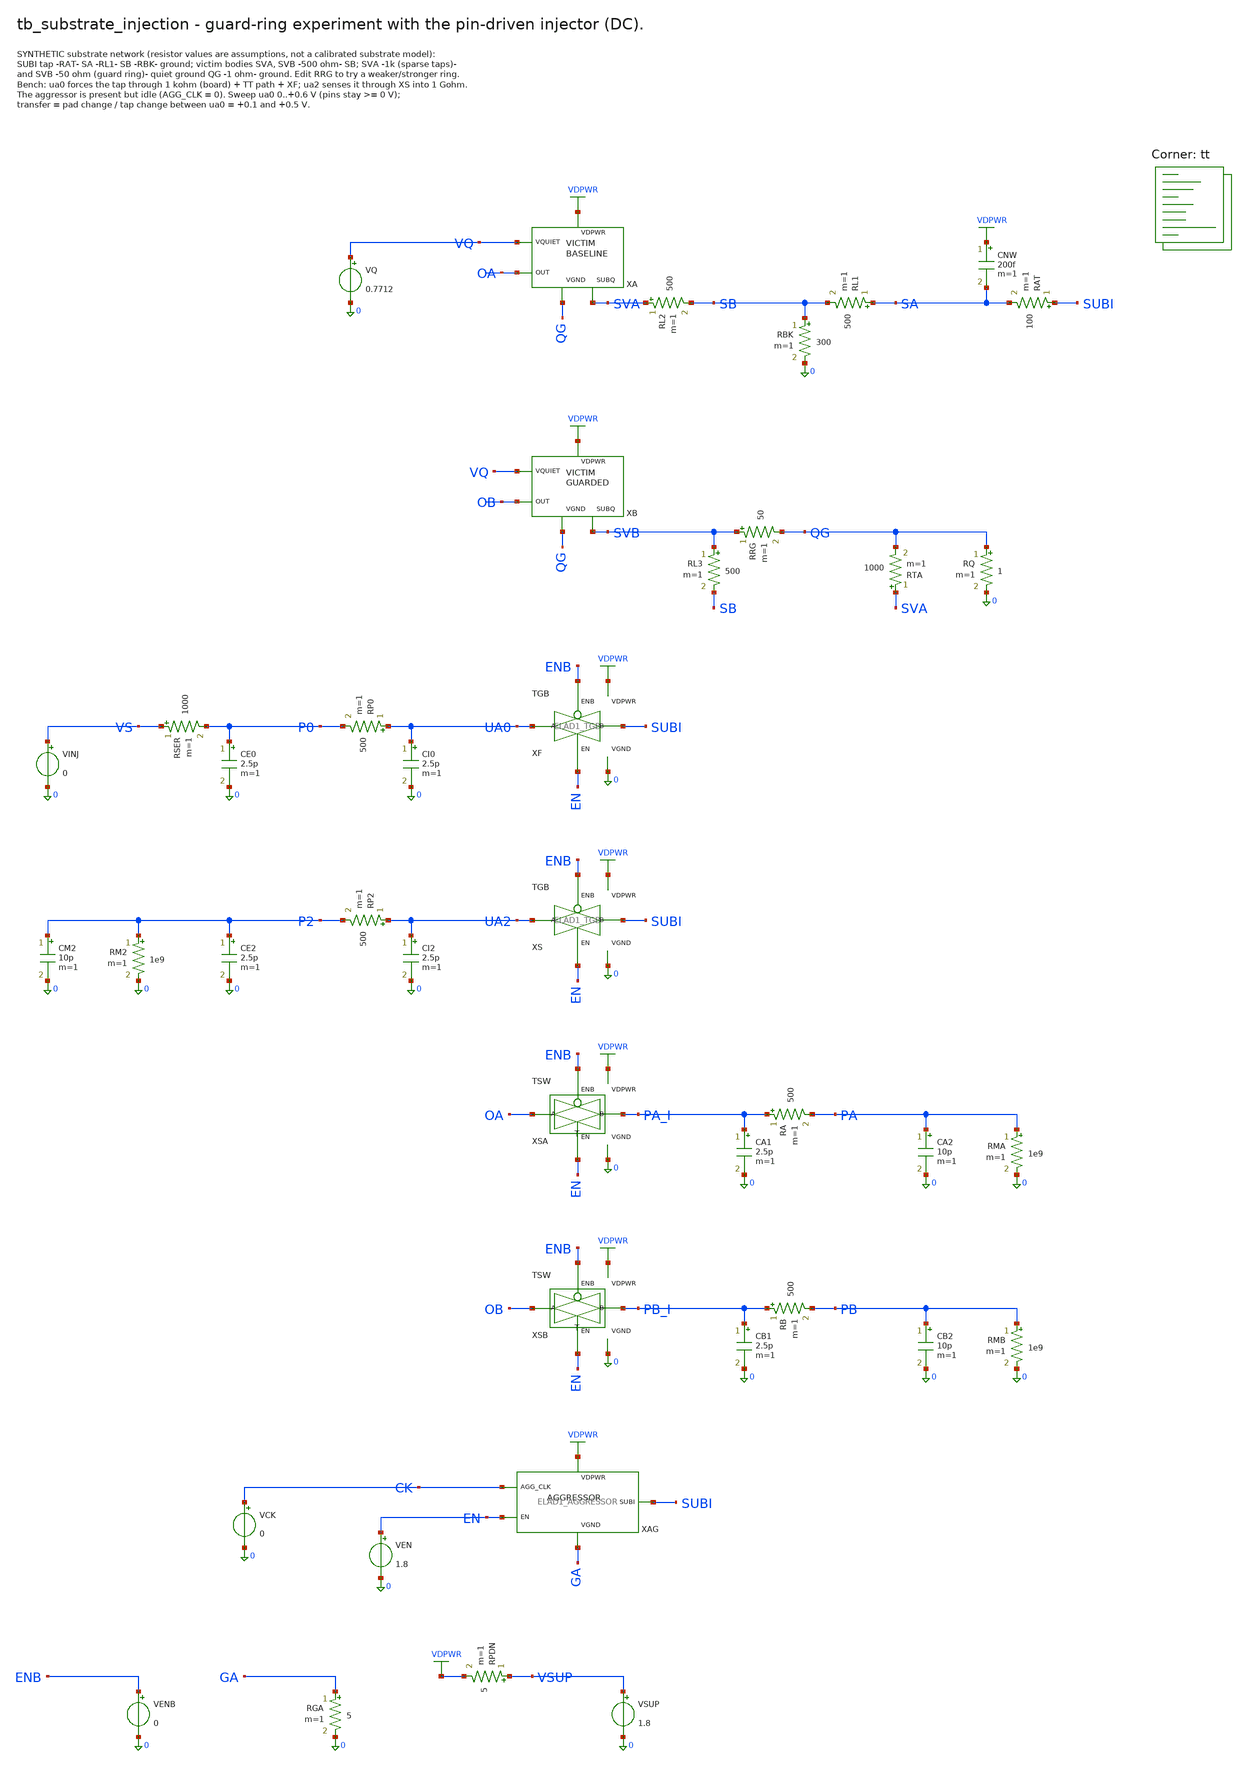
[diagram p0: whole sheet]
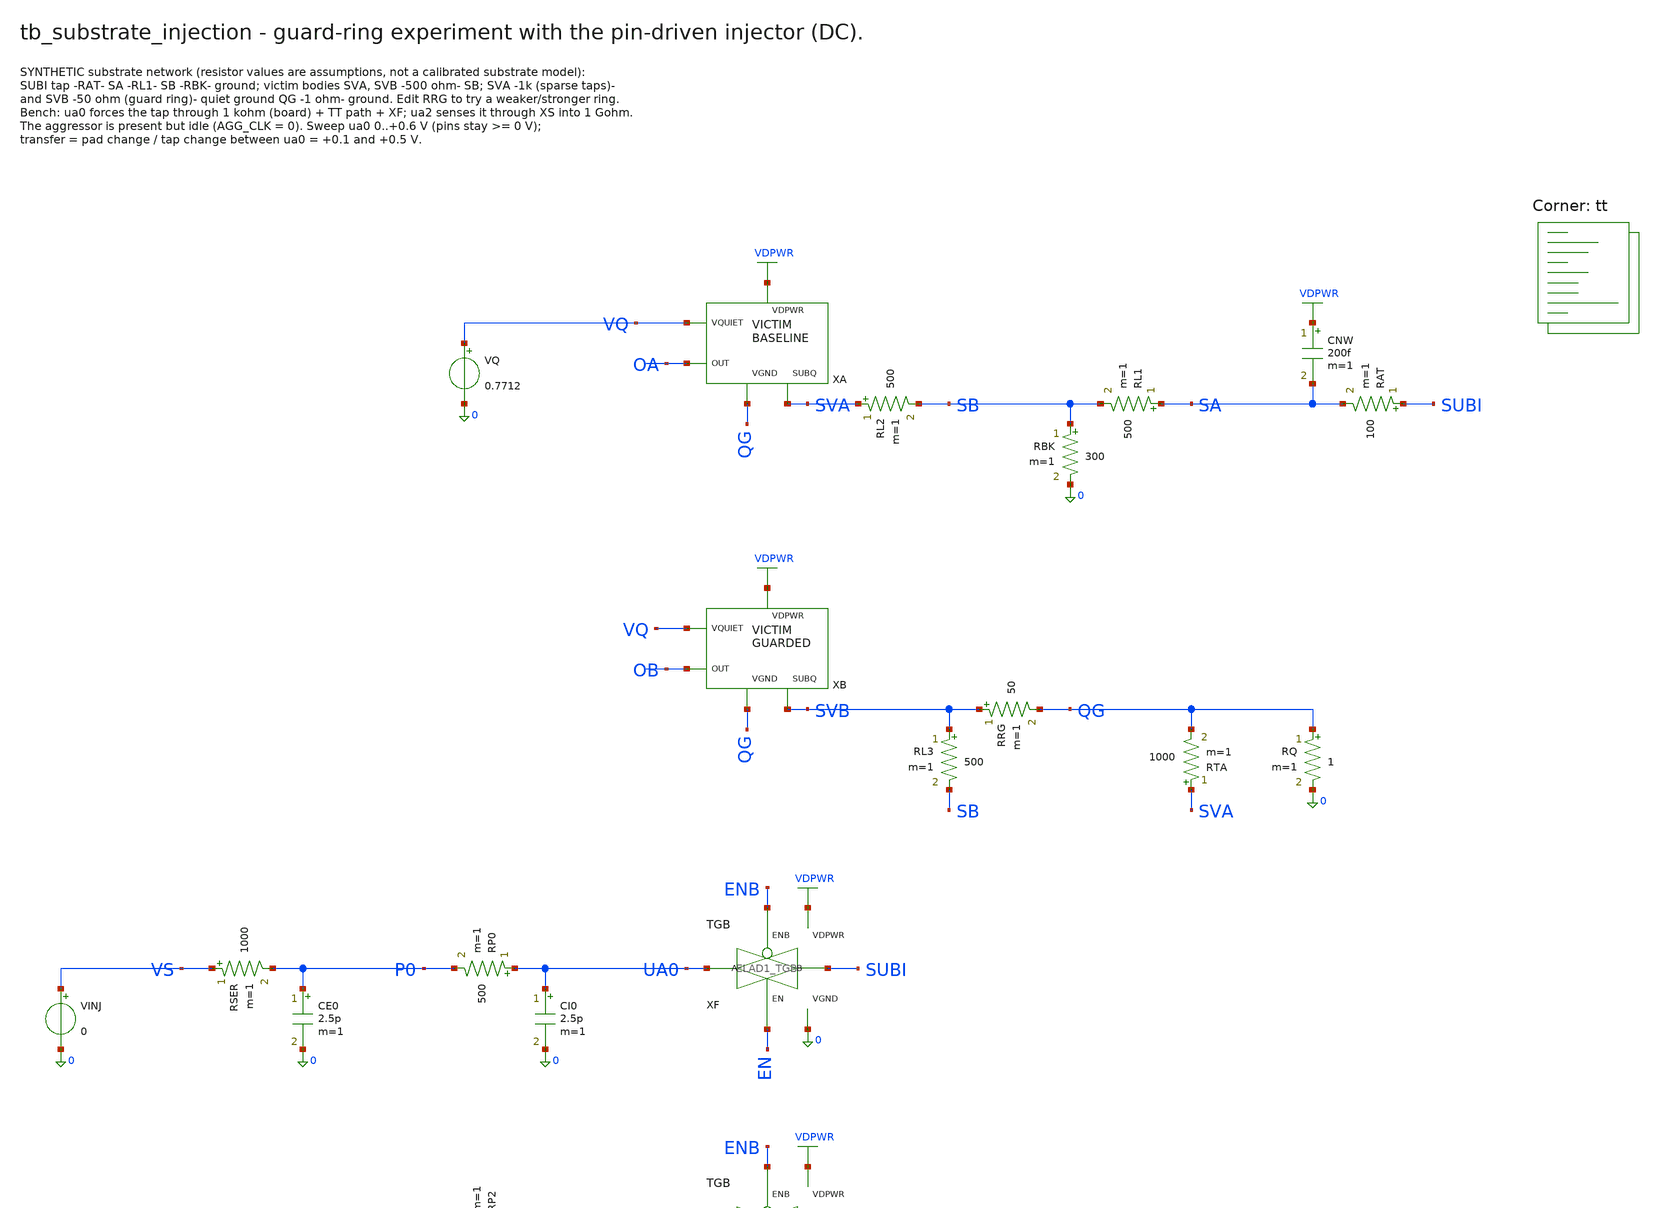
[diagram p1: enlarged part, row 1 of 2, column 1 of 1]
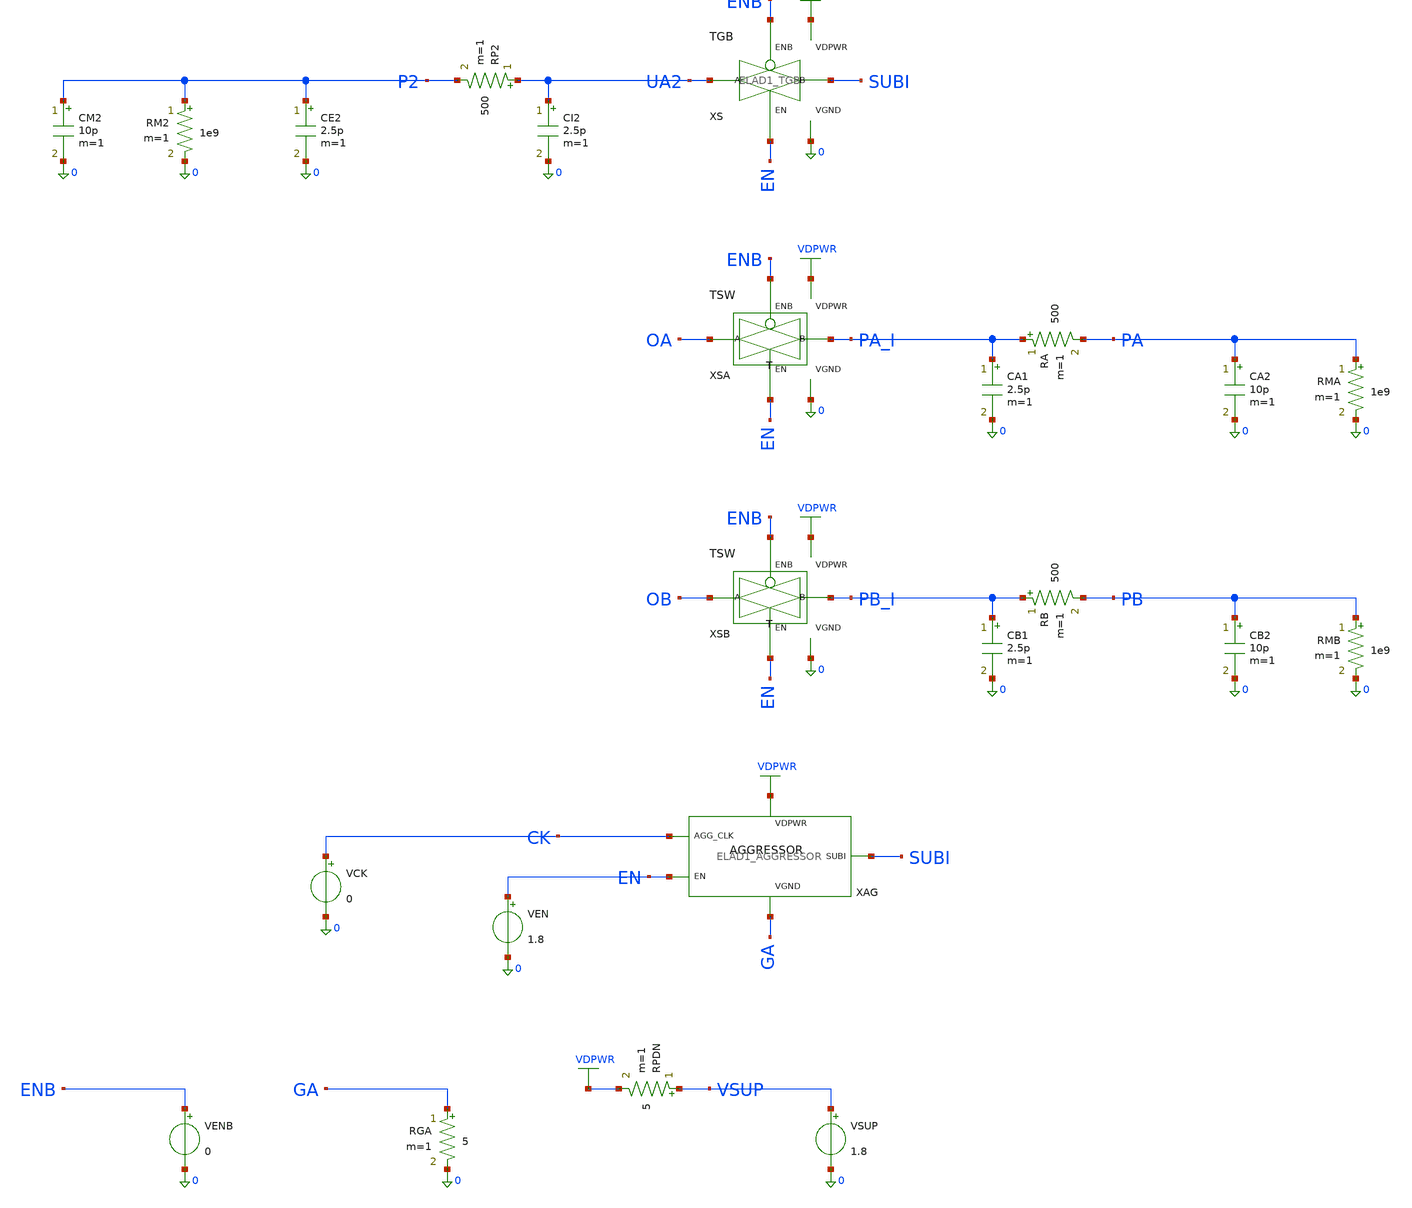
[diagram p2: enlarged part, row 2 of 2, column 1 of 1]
** sch_path: cells/ELAD1_AGGRESSOR/schematic/tb_substrate_injection.sch
**.subckt tb_substrate_injection
XA VQ OA VDPWR QG SVA ELAD1_VICTIM_BASELINE
VQ VQ 0 0.7712
RL2 SVA SB 500 m=1
RBK SB 0 300 m=1
RL1 SA SB 500 m=1
CNW VDPWR SA 200f m=1
RAT SUBI SA 100 m=1
XB VQ OB VDPWR QG SVB ELAD1_VICTIM_GUARDED
RL3 SVB SB 500 m=1
RRG SVB QG 50 m=1
RTA SVA QG 1000 m=1
RQ QG 0 1 m=1
XF UA0 SUBI EN ENB VDPWR 0 ELAD1_TGB
CI0 UA0 0 2.5p m=1
RP0 UA0 P0 500 m=1
CE0 P0 0 2.5p m=1
RSER VS P0 1000 m=1
VINJ VS 0 0
XS UA2 SUBI EN ENB VDPWR 0 ELAD1_TGB
CI2 UA2 0 2.5p m=1
RP2 UA2 P2 500 m=1
CE2 P2 0 2.5p m=1
RM2 P2 0 1e9 m=1
CM2 P2 0 10p m=1
XSA OA PA_I EN ENB VDPWR 0 ELAD1_TSW
CA1 PA_I 0 2.5p m=1
RA PA_I PA 500 m=1
CA2 PA 0 10p m=1
RMA PA 0 1e9 m=1
XSB OB PB_I EN ENB VDPWR 0 ELAD1_TSW
CB1 PB_I 0 2.5p m=1
RB PB_I PB 500 m=1
CB2 PB 0 10p m=1
RMB PB 0 1e9 m=1
XAG CK EN VDPWR GA SUBI ELAD1_AGGRESSOR
VEN EN 0 1.8
VCK CK 0 0
VENB ENB 0 0
RGA GA 0 5 m=1
RPDN VSUP VDPWR 5 m=1
VSUP VSUP 0 1.8
**** begin user architecture code

.option gmin=1e-15 reltol=1e-6 abstol=1e-15 vntol=1e-8
.control
dc VINJ 0 0.6 0.05
meas dc ph find v(P2) at=0.5
meas dc pl find v(P2) at=0.1
meas dc th find v(SUBI) at=0.5
meas dc ah find v(PA) at=0.5
meas dc al find v(PA) at=0.1
meas dc bh find v(PB) at=0.5
meas dc bl find v(PB) at=0.1
meas dc z find v(SUBI) at=0
let t_a = (ah-al)/(ph-pl)
let t_b = (bh-bl)/(ph-pl)
let ratio = t_a/t_b
let sense_err = abs(ph-th)
let tap0 = abs(z)
echo ROW inject tap_hi=$&ph t_a=$&t_a t_b=$&t_b ratio=$&ratio sense_err=$&sense_err tap0=$&tap0
.endc

.lib $::SKYWATER_MODELS/sky130.lib.spice tt
**** end user architecture code
**.ends

* expanding   symbol:  ELAD1_VICTIM_BASELINE.sym # of pins=5
** sym_path: cells/ELAD1_VICTIM_BASELINE/schematic/ELAD1_VICTIM_BASELINE.sym
** sch_path: cells/ELAD1_VICTIM_BASELINE/schematic/ELAD1_VICTIM_BASELINE.sch
.subckt ELAD1_VICTIM_BASELINE VQUIET OUT VDPWR VGND SUBQ
*.iopin VQUIET
*.iopin OUT
*.iopin VDPWR
*.iopin VGND
*.iopin SUBQ
XMVIC[1] OUT VQUIET VGND SUBQ sky130_fd_pr__nfet_01v8 L=1 W=1 nf=1 ad='int((1 + 1)/2) * 1 / 1 * 0.29'
+ as='int((1 + 2)/2) * 1 / 1 * 0.29' pd='2*int((1 + 1)/2) * (1 / 1 + 0.29)' ps='2*int((1 + 2)/2) * (1 / 1 + 0.29)'
+ nrd='0.29 / 1 ' nrs='0.29 / 1 ' sa=0 sb=0 sd=0 mult=1 m=1
XMVIC[0] OUT VQUIET VGND SUBQ sky130_fd_pr__nfet_01v8 L=1 W=1 nf=1 ad='int((1 + 1)/2) * 1 / 1 * 0.29'
+ as='int((1 + 2)/2) * 1 / 1 * 0.29' pd='2*int((1 + 1)/2) * (1 / 1 + 0.29)' ps='2*int((1 + 2)/2) * (1 / 1 + 0.29)'
+ nrd='0.29 / 1 ' nrs='0.29 / 1 ' sa=0 sb=0 sd=0 mult=1 m=1
XMD[1] VGND VGND VGND SUBQ sky130_fd_pr__nfet_01v8 L=1 W=1 nf=1 ad='int((1 + 1)/2) * 1 / 1 * 0.29' as='int((1 + 2)/2) * 1 / 1 * 0.29'
+ pd='2*int((1 + 1)/2) * (1 / 1 + 0.29)' ps='2*int((1 + 2)/2) * (1 / 1 + 0.29)' nrd='0.29 / 1 ' nrs='0.29 / 1 '
+ sa=0 sb=0 sd=0 mult=2 m=2
XMD[0] VGND VGND VGND SUBQ sky130_fd_pr__nfet_01v8 L=1 W=1 nf=1 ad='int((1 + 1)/2) * 1 / 1 * 0.29' as='int((1 + 2)/2) * 1 / 1 * 0.29'
+ pd='2*int((1 + 1)/2) * (1 / 1 + 0.29)' ps='2*int((1 + 2)/2) * (1 / 1 + 0.29)' nrd='0.29 / 1 ' nrs='0.29 / 1 '
+ sa=0 sb=0 sd=0 mult=2 m=2
XR1 OUT VDPWR SUBQ sky130_fd_pr__res_xhigh_po_0p69 L=31.7 mult=1 m=1
.ends


* expanding   symbol:  ELAD1_VICTIM_GUARDED.sym # of pins=5
** sym_path: cells/ELAD1_VICTIM_GUARDED/schematic/ELAD1_VICTIM_GUARDED.sym
** sch_path: cells/ELAD1_VICTIM_GUARDED/schematic/ELAD1_VICTIM_GUARDED.sch
.subckt ELAD1_VICTIM_GUARDED VQUIET OUT VDPWR VGND SUBQ
*.iopin VQUIET
*.iopin OUT
*.iopin VDPWR
*.iopin VGND
*.iopin SUBQ
XRLD VDPWR OUT SUBQ sky130_fd_pr__res_xhigh_po W=0.69 L=31.7 mult=1 m=1
XMVIC OUT VQUIET VGND SUBQ sky130_fd_pr__nfet_01v8 L=1 W=2 nf=1 ad='int((1 + 1)/2) * 2 / 1 * 0.29' as='int((1 + 2)/2) * 2 / 1 * 0.29'
+ pd='2*int((1 + 1)/2) * (2 / 1 + 0.29)' ps='2*int((1 + 2)/2) * (2 / 1 + 0.29)' nrd='0.29 / 2 ' nrs='0.29 / 2 '
+ sa=0 sb=0 sd=0 mult=1 m=1
XDUM[1] VGND VGND VGND SUBQ sky130_fd_pr__nfet_01v8 L=1 W=2 nf=1 ad='int((1 + 1)/2) * 2 / 1 * 0.29' as='int((1 + 2)/2) * 2 / 1 * 0.29'
+ pd='2*int((1 + 1)/2) * (2 / 1 + 0.29)' ps='2*int((1 + 2)/2) * (2 / 1 + 0.29)' nrd='0.29 / 2 ' nrs='0.29 / 2 '
+ sa=0 sb=0 sd=0 mult=1 m=1
XDUM[0] VGND VGND VGND SUBQ sky130_fd_pr__nfet_01v8 L=1 W=2 nf=1 ad='int((1 + 1)/2) * 2 / 1 * 0.29' as='int((1 + 2)/2) * 2 / 1 * 0.29'
+ pd='2*int((1 + 1)/2) * (2 / 1 + 0.29)' ps='2*int((1 + 2)/2) * (2 / 1 + 0.29)' nrd='0.29 / 2 ' nrs='0.29 / 2 '
+ sa=0 sb=0 sd=0 mult=1 m=1
.ends


* expanding   symbol:  ELAD1_TGB.sym # of pins=6
** sym_path: cells/ELAD1_TGB/schematic/ELAD1_TGB.sym
** sch_path: cells/ELAD1_TGB/schematic/ELAD1_TGB.sch
.subckt ELAD1_TGB A B EN ENB VDPWR VGND
*.iopin A
*.iopin B
*.iopin EN
*.iopin ENB
*.iopin VDPWR
*.iopin VGND
XMN A EN B VGND sky130_fd_pr__nfet_01v8 L=0.15 W=1 nf=1 ad='int((1 + 1)/2) * 1 / 1 * 0.29' as='int((1 + 2)/2) * 1 / 1 * 0.29'
+ pd='2*int((1 + 1)/2) * (1 / 1 + 0.29)' ps='2*int((1 + 2)/2) * (1 / 1 + 0.29)' nrd='0.29 / 1 ' nrs='0.29 / 1 '
+ sa=0 sb=0 sd=0 mult=1 m=1
XMP A ENB B VDPWR sky130_fd_pr__pfet_01v8 L=0.15 W=2 nf=1 ad='int((nf+1)/2) * W/nf * 0.29' as='int((nf+2)/2) * W/nf * 0.29'
+ pd='2*int((nf+1)/2) * (W/nf + 0.29)' ps='2*int((nf+2)/2) * (W/nf + 0.29)' nrd='0.29 / W' nrs='0.29 / W'
+ sa=0 sb=0 sd=0 mult=1 m=1
.ends


* expanding   symbol:  ELAD1_TSW.sym # of pins=6
** sym_path: cells/ELAD1_TSW/schematic/ELAD1_TSW.sym
** sch_path: cells/ELAD1_TSW/schematic/ELAD1_TSW.sch
.subckt ELAD1_TSW A B EN ENB VDPWR VGND
*.iopin A
*.iopin B
*.iopin EN
*.iopin ENB
*.iopin VDPWR
*.iopin VGND
x1 A M EN ENB VDPWR VGND ELAD1_TGA
x1 M B EN ENB VDPWR VGND ELAD1_TGA
XMN1 M ENB VGND VGND sky130_fd_pr__nfet_01v8 L=0.15 W=1 nf=1 ad='int((1 + 1)/2) * 1 / 1 * 0.29' as='int((1 + 2)/2) * 1 / 1 * 0.29'
+ pd='2*int((1 + 1)/2) * (1 / 1 + 0.29)' ps='2*int((1 + 2)/2) * (1 / 1 + 0.29)' nrd='0.29 / 1 ' nrs='0.29 / 1 '
+ sa=0 sb=0 sd=0 mult=1 m=1
.ends


* expanding   symbol:  ELAD1_AGGRESSOR.sym # of pins=5
** sym_path: cells/ELAD1_AGGRESSOR/schematic/ELAD1_AGGRESSOR.sym
** sch_path: cells/ELAD1_AGGRESSOR/schematic/ELAD1_AGGRESSOR.sch
.subckt ELAD1_AGGRESSOR AGG_CLK EN VDPWR VGND SUBI
*.iopin AGG_CLK
*.iopin EN
*.iopin VDPWR
*.iopin VGND
*.iopin SUBI
XIC AGG_CLK CKB VDPWR VGND ELAD1_INV
XIE EN ENB VDPWR VGND ELAD1_INV
XGIP1 gip ENB VDPWR VDPWR sky130_fd_pr__pfet_01v8 L=0.15 W=2 nf=1 ad='int((nf+1)/2) * W/nf * 0.29' as='int((nf+2)/2) * W/nf * 0.29'
+ pd='2*int((nf+1)/2) * (W/nf + 0.29)' ps='2*int((nf+2)/2) * (W/nf + 0.29)' nrd='0.29 / W' nrs='0.29 / W'
+ sa=0 sb=0 sd=0 mult=1 m=1
XGIP2 GI CKB gip VDPWR sky130_fd_pr__pfet_01v8 L=0.15 W=2 nf=1 ad='int((nf+1)/2) * W/nf * 0.29' as='int((nf+2)/2) * W/nf * 0.29'
+ pd='2*int((nf+1)/2) * (W/nf + 0.29)' ps='2*int((nf+2)/2) * (W/nf + 0.29)' nrd='0.29 / W' nrs='0.29 / W'
+ sa=0 sb=0 sd=0 mult=1 m=1
XGIN1 GI ENB VGND VGND sky130_fd_pr__nfet_01v8 L=1 W=0.42 nf=1 ad='int((1 + 1)/2) * 0.42 / 1 * 0.29'
+ as='int((1 + 2)/2) * 0.42 / 1 * 0.29' pd='2*int((1 + 1)/2) * (0.42 / 1 + 0.29)' ps='2*int((1 + 2)/2) * (0.42 / 1 + 0.29)'
+ nrd='0.29 / 0.42 ' nrs='0.29 / 0.42 ' sa=0 sb=0 sd=0 mult=1 m=1
XGIN2 GI CKB VGND VGND sky130_fd_pr__nfet_01v8 L=1 W=0.42 nf=1 ad='int((1 + 1)/2) * 0.42 / 1 * 0.29'
+ as='int((1 + 2)/2) * 0.42 / 1 * 0.29' pd='2*int((1 + 1)/2) * (0.42 / 1 + 0.29)' ps='2*int((1 + 2)/2) * (0.42 / 1 + 0.29)'
+ nrd='0.29 / 0.42 ' nrs='0.29 / 0.42 ' sa=0 sb=0 sd=0 mult=1 m=1
XGDP1 gdp ENB VDPWR VDPWR sky130_fd_pr__pfet_01v8 L=0.15 W=2 nf=1 ad='int((nf+1)/2) * W/nf * 0.29' as='int((nf+2)/2) * W/nf * 0.29'
+ pd='2*int((nf+1)/2) * (W/nf + 0.29)' ps='2*int((nf+2)/2) * (W/nf + 0.29)' nrd='0.29 / W' nrs='0.29 / W'
+ sa=0 sb=0 sd=0 mult=1 m=1
XGDP2 GD AGG_CLK gdp VDPWR sky130_fd_pr__pfet_01v8 L=0.15 W=2 nf=1 ad='int((nf+1)/2) * W/nf * 0.29' as='int((nf+2)/2) * W/nf * 0.29'
+ pd='2*int((nf+1)/2) * (W/nf + 0.29)' ps='2*int((nf+2)/2) * (W/nf + 0.29)' nrd='0.29 / W' nrs='0.29 / W'
+ sa=0 sb=0 sd=0 mult=1 m=1
XGDN1 GD ENB VGND VGND sky130_fd_pr__nfet_01v8 L=1 W=0.42 nf=1 ad='int((1 + 1)/2) * 0.42 / 1 * 0.29'
+ as='int((1 + 2)/2) * 0.42 / 1 * 0.29' pd='2*int((1 + 1)/2) * (0.42 / 1 + 0.29)' ps='2*int((1 + 2)/2) * (0.42 / 1 + 0.29)'
+ nrd='0.29 / 0.42 ' nrs='0.29 / 0.42 ' sa=0 sb=0 sd=0 mult=1 m=1
XGDN2 GD AGG_CLK VGND VGND sky130_fd_pr__nfet_01v8 L=1 W=0.42 nf=1 ad='int((1 + 1)/2) * 0.42 / 1 * 0.29'
+ as='int((1 + 2)/2) * 0.42 / 1 * 0.29' pd='2*int((1 + 1)/2) * (0.42 / 1 + 0.29)' ps='2*int((1 + 2)/2) * (0.42 / 1 + 0.29)'
+ nrd='0.29 / 0.42 ' nrs='0.29 / 0.42 ' sa=0 sb=0 sd=0 mult=1 m=1
XRL X VDPWR VGND sky130_fd_pr__res_xhigh_po W=0.69 L=7.3 mult=1 m=1
XMINJ X GI SUBI VGND sky130_fd_pr__nfet_01v8 L=0.15 W=2 nf=1 ad='int((1 + 1)/2) * 2 / 1 * 0.29' as='int((1 + 2)/2) * 2 / 1 * 0.29'
+ pd='2*int((1 + 1)/2) * (2 / 1 + 0.29)' ps='2*int((1 + 2)/2) * (2 / 1 + 0.29)' nrd='0.29 / 2 ' nrs='0.29 / 2 '
+ sa=0 sb=0 sd=0 mult=1 m=1
XMDUM X GD D VGND sky130_fd_pr__nfet_01v8 L=0.15 W=2 nf=1 ad='int((1 + 1)/2) * 2 / 1 * 0.29' as='int((1 + 2)/2) * 2 / 1 * 0.29'
+ pd='2*int((1 + 1)/2) * (2 / 1 + 0.29)' ps='2*int((1 + 2)/2) * (2 / 1 + 0.29)' nrd='0.29 / 2 ' nrs='0.29 / 2 '
+ sa=0 sb=0 sd=0 mult=1 m=1
XRDUM VGND D sky130_fd_pr__res_generic_po W=1 L=15 m=1
.ends


* expanding   symbol:  ELAD1_TGA.sym # of pins=6
** sym_path: cells/ELAD1_TGA/schematic/ELAD1_TGA.sym
** sch_path: cells/ELAD1_TGA/schematic/ELAD1_TGA.sch
.subckt ELAD1_TGA A B EN ENB VDPWR VGND
*.iopin A
*.iopin B
*.iopin EN
*.iopin ENB
*.iopin VDPWR
*.iopin VGND
XMN A EN B VGND sky130_fd_pr__nfet_01v8_lvt L=0.15 W=4 nf=1 ad='int((1 + 1)/2) * 4 / 1 * 0.29' as='int((1 + 2)/2) * 4 / 1 * 0.29'
+ pd='2*int((1 + 1)/2) * (4 / 1 + 0.29)' ps='2*int((1 + 2)/2) * (4 / 1 + 0.29)' nrd='0.29 / 4 ' nrs='0.29 / 4 '
+ sa=0 sb=0 sd=0 mult=1 m=1
XMP A ENB B VDPWR sky130_fd_pr__pfet_01v8_lvt L=0.35 W=12 nf=1 ad='int((1 + 1)/2) * 12 / 1 * 0.29' as='int((1 + 2)/2) * 12 / 1 * 0.29'
+ pd='2*int((1 + 1)/2) * (12 / 1 + 0.29)' ps='2*int((1 + 2)/2) * (12 / 1 + 0.29)' nrd='0.29 / 12 ' nrs='0.29 / 12 '
+ sa=0 sb=0 sd=0 mult=1 m=1
.ends


* expanding   symbol:  ELAD1_INV.sym # of pins=4
** sym_path: cells/ELAD1_INV/schematic/ELAD1_INV.sym
** sch_path: cells/ELAD1_INV/schematic/ELAD1_INV.sch
.subckt ELAD1_INV A Y VDPWR VGND
*.iopin A
*.iopin Y
*.iopin VDPWR
*.iopin VGND
XMN Y A VGND VGND sky130_fd_pr__nfet_01v8 L=0.15 W=0.65 nf=1 ad='int((1 + 1)/2) * 0.65 / 1 * 0.29' as='int((1 + 2)/2) * 0.65 / 1 * 0.29'
+ pd='2*int((1 + 1)/2) * (0.65 / 1 + 0.29)' ps='2*int((1 + 2)/2) * (0.65 / 1 + 0.29)' nrd='0.29 / 0.65 '
+ nrs='0.29 / 0.65 ' sa=0 sb=0 sd=0 mult=1 m=1
XMP Y A VDPWR VDPWR sky130_fd_pr__pfet_01v8 L=0.15 W=1 nf=1 ad='int((nf+1)/2) * W/nf * 0.29' as='int((nf+2)/2) * W/nf * 0.29'
+ pd='2*int((nf+1)/2) * (W/nf + 0.29)' ps='2*int((nf+2)/2) * (W/nf + 0.29)' nrd='0.29 / W' nrs='0.29 / W'
+ sa=0 sb=0 sd=0 mult=1 m=1
.ends

.GLOBAL VGND
.GLOBAL VDPWR
.end
